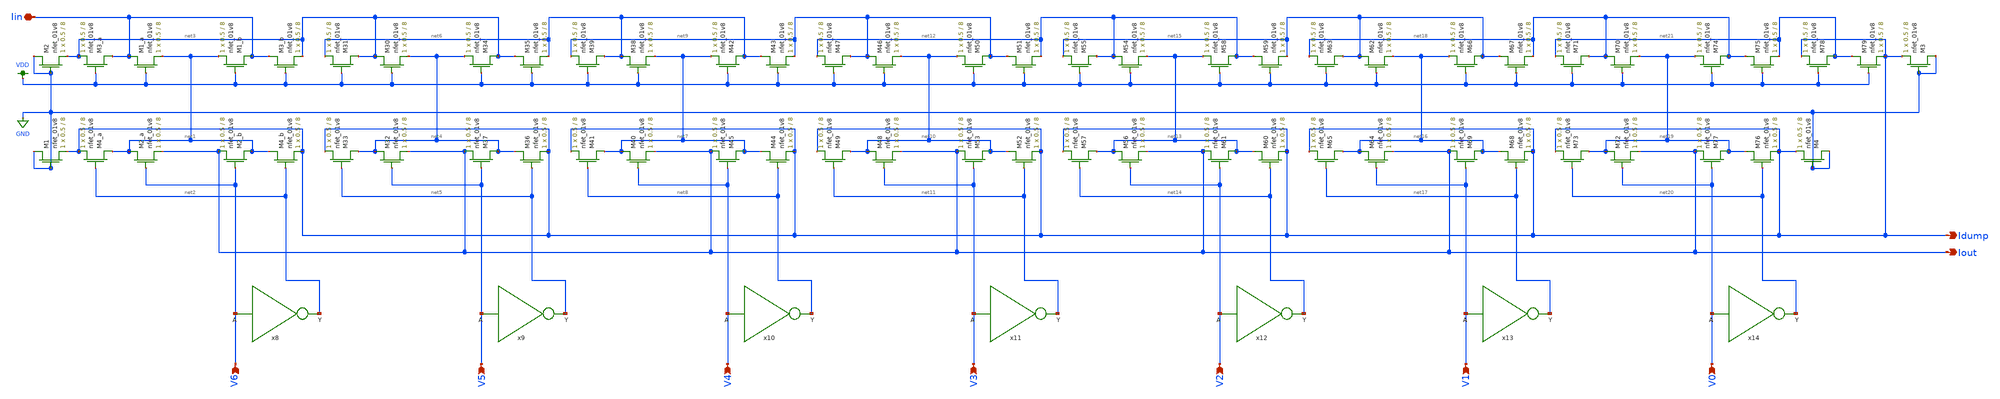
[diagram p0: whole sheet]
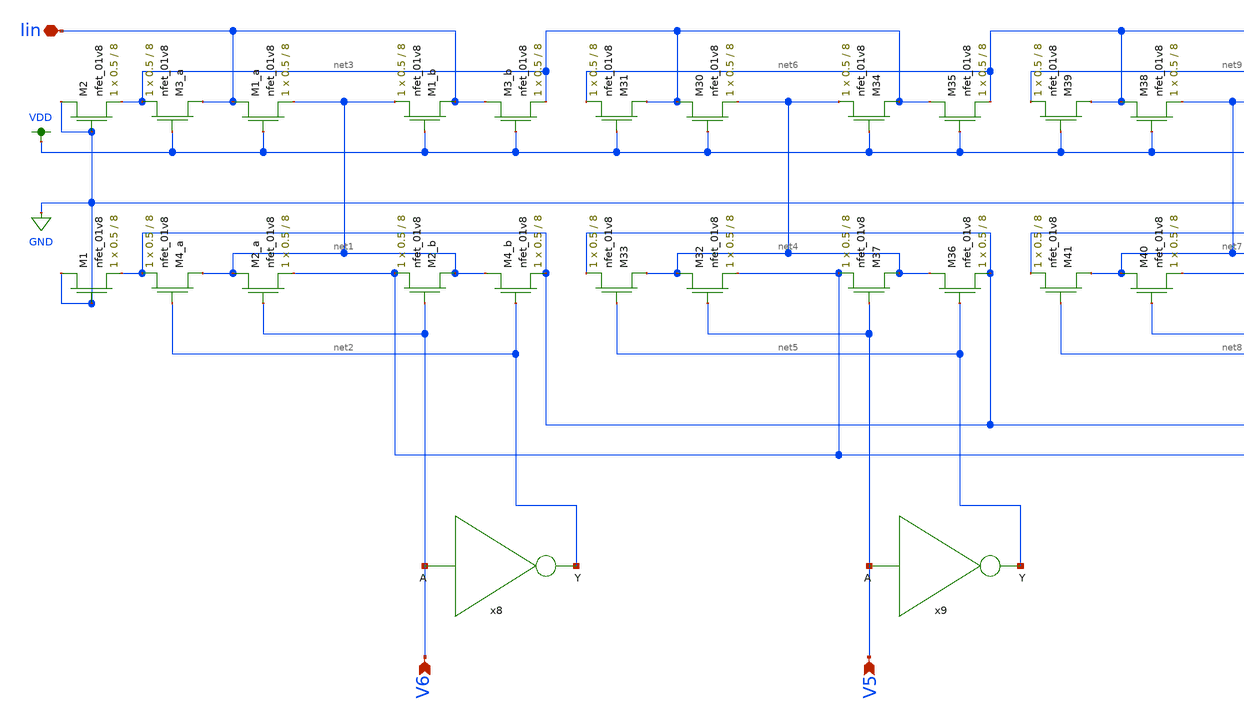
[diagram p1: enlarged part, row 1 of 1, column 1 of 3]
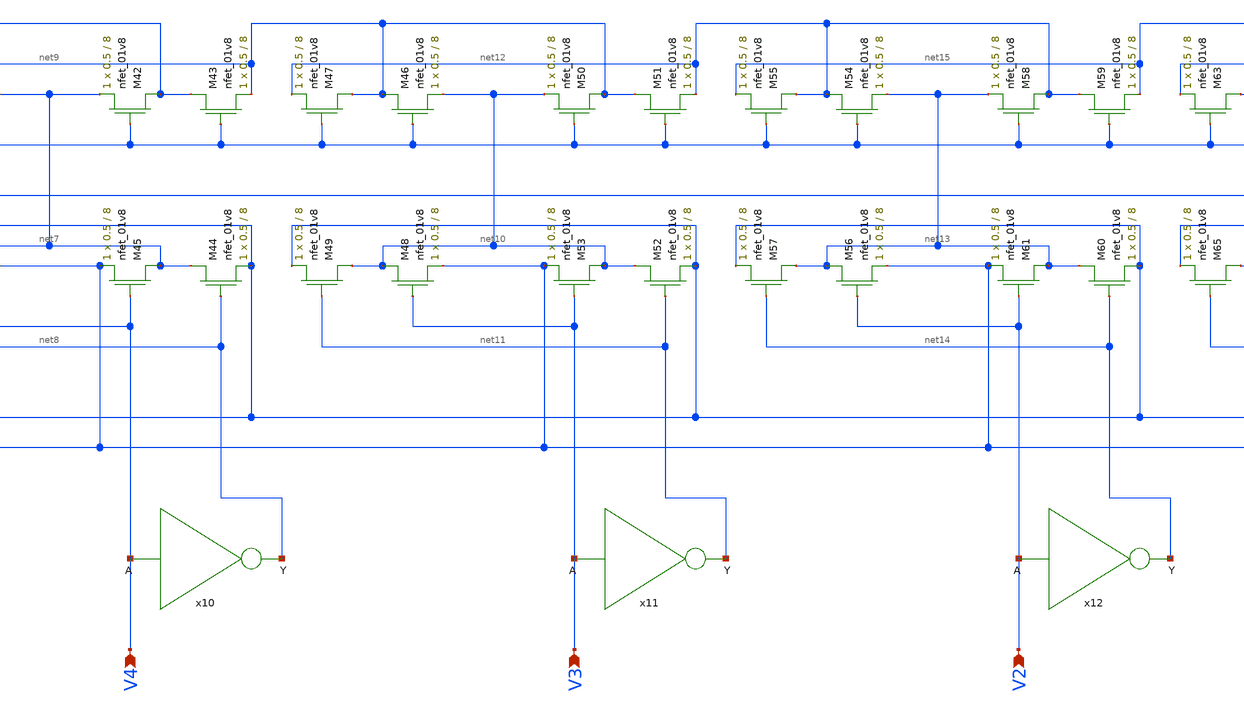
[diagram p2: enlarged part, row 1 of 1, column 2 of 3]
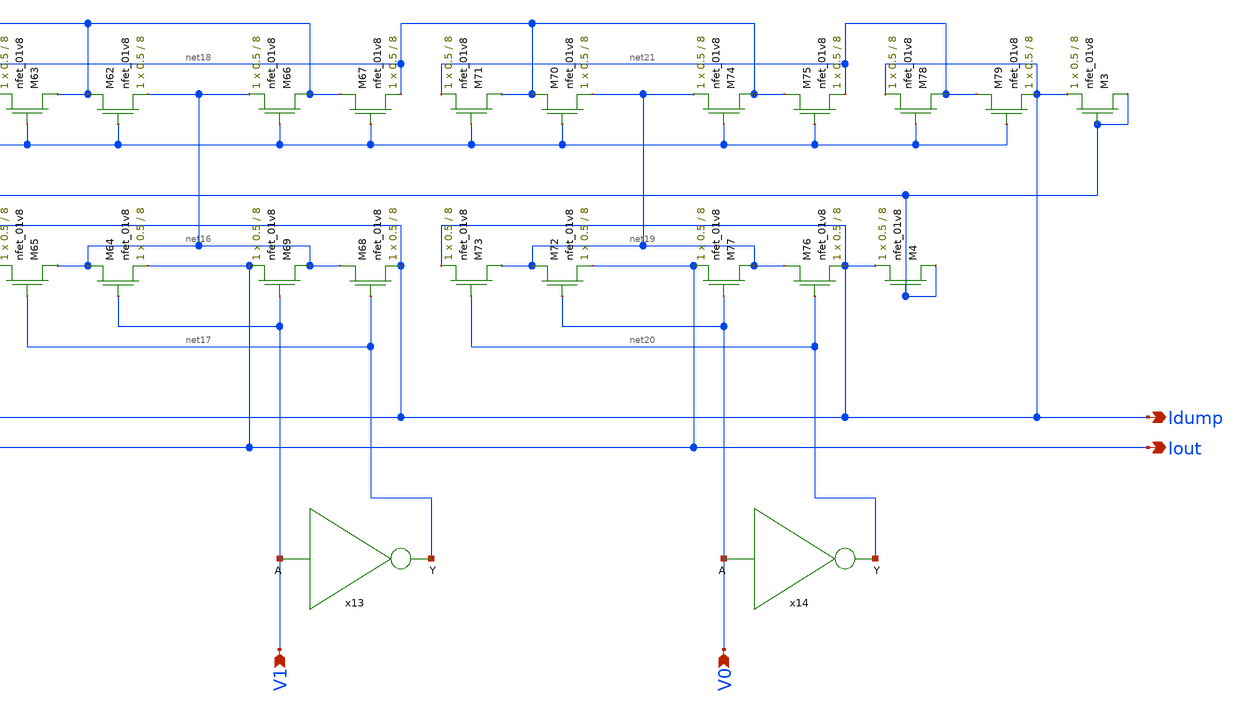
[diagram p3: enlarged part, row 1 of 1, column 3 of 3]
** sch_path: xschem/ladder_lds.sch
**.subckt ladder_lds Iin Idump Iout V6 V5 V4 V3 V2 V1 V0
*.iopin Iin
*.opin Idump
*.opin Iout
*.ipin V6
*.ipin V5
*.ipin V4
*.ipin V3
*.ipin V2
*.ipin V1
*.ipin V0
XM1_a Iin VDD net1 GND sky130_fd_pr__nfet_01v8 L=8 W=0.5 nf=1 ad='int((nf+1)/2) * W/nf * 0.29' as='int((nf+2)/2) * W/nf * 0.29'
+ pd='2*int((nf+1)/2) * (W/nf + 0.29)' ps='2*int((nf+2)/2) * (W/nf + 0.29)' nrd='0.29 / W' nrs='0.29 / W'
+ sa=0 sb=0 sd=0 mult=1 m=1
XM3_a Iin VDD net3 GND sky130_fd_pr__nfet_01v8 L=8 W=0.5 nf=1 ad='int((nf+1)/2) * W/nf * 0.29' as='int((nf+2)/2) * W/nf * 0.29'
+ pd='2*int((nf+1)/2) * (W/nf + 0.29)' ps='2*int((nf+2)/2) * (W/nf + 0.29)' nrd='0.29 / W' nrs='0.29 / W'
+ sa=0 sb=0 sd=0 mult=1 m=1
XM2_a net1 V6 Iout GND sky130_fd_pr__nfet_01v8 L=8 W=0.5 nf=1 ad='int((nf+1)/2) * W/nf * 0.29' as='int((nf+2)/2) * W/nf * 0.29'
+ pd='2*int((nf+1)/2) * (W/nf + 0.29)' ps='2*int((nf+2)/2) * (W/nf + 0.29)' nrd='0.29 / W' nrs='0.29 / W'
+ sa=0 sb=0 sd=0 mult=1 m=1
XM4_a net1 net2 Idump GND sky130_fd_pr__nfet_01v8 L=8 W=0.5 nf=1 ad='int((nf+1)/2) * W/nf * 0.29' as='int((nf+2)/2) * W/nf * 0.29'
+ pd='2*int((nf+1)/2) * (W/nf + 0.29)' ps='2*int((nf+2)/2) * (W/nf + 0.29)' nrd='0.29 / W' nrs='0.29 / W'
+ sa=0 sb=0 sd=0 mult=1 m=1
XM1_b Iin VDD net1 GND sky130_fd_pr__nfet_01v8 L=8 W=0.5 nf=1 ad='int((nf+1)/2) * W/nf * 0.29' as='int((nf+2)/2) * W/nf * 0.29'
+ pd='2*int((nf+1)/2) * (W/nf + 0.29)' ps='2*int((nf+2)/2) * (W/nf + 0.29)' nrd='0.29 / W' nrs='0.29 / W'
+ sa=0 sb=0 sd=0 mult=1 m=1
XM3_b Iin VDD net3 GND sky130_fd_pr__nfet_01v8 L=8 W=0.5 nf=1 ad='int((nf+1)/2) * W/nf * 0.29' as='int((nf+2)/2) * W/nf * 0.29'
+ pd='2*int((nf+1)/2) * (W/nf + 0.29)' ps='2*int((nf+2)/2) * (W/nf + 0.29)' nrd='0.29 / W' nrs='0.29 / W'
+ sa=0 sb=0 sd=0 mult=1 m=1
XM4_b net1 net2 Idump GND sky130_fd_pr__nfet_01v8 L=8 W=0.5 nf=1 ad='int((nf+1)/2) * W/nf * 0.29' as='int((nf+2)/2) * W/nf * 0.29'
+ pd='2*int((nf+1)/2) * (W/nf + 0.29)' ps='2*int((nf+2)/2) * (W/nf + 0.29)' nrd='0.29 / W' nrs='0.29 / W'
+ sa=0 sb=0 sd=0 mult=1 m=1
XM2_b net1 V6 Iout GND sky130_fd_pr__nfet_01v8 L=8 W=0.5 nf=1 ad='int((nf+1)/2) * W/nf * 0.29' as='int((nf+2)/2) * W/nf * 0.29'
+ pd='2*int((nf+1)/2) * (W/nf + 0.29)' ps='2*int((nf+2)/2) * (W/nf + 0.29)' nrd='0.29 / W' nrs='0.29 / W'
+ sa=0 sb=0 sd=0 mult=1 m=1
XM30 net3 VDD net4 GND sky130_fd_pr__nfet_01v8 L=8 W=0.5 nf=1 ad='int((nf+1)/2) * W/nf * 0.29' as='int((nf+2)/2) * W/nf * 0.29'
+ pd='2*int((nf+1)/2) * (W/nf + 0.29)' ps='2*int((nf+2)/2) * (W/nf + 0.29)' nrd='0.29 / W' nrs='0.29 / W'
+ sa=0 sb=0 sd=0 mult=1 m=1
XM31 net3 VDD net6 GND sky130_fd_pr__nfet_01v8 L=8 W=0.5 nf=1 ad='int((nf+1)/2) * W/nf * 0.29' as='int((nf+2)/2) * W/nf * 0.29'
+ pd='2*int((nf+1)/2) * (W/nf + 0.29)' ps='2*int((nf+2)/2) * (W/nf + 0.29)' nrd='0.29 / W' nrs='0.29 / W'
+ sa=0 sb=0 sd=0 mult=1 m=1
XM32 net4 V5 Iout GND sky130_fd_pr__nfet_01v8 L=8 W=0.5 nf=1 ad='int((nf+1)/2) * W/nf * 0.29' as='int((nf+2)/2) * W/nf * 0.29'
+ pd='2*int((nf+1)/2) * (W/nf + 0.29)' ps='2*int((nf+2)/2) * (W/nf + 0.29)' nrd='0.29 / W' nrs='0.29 / W'
+ sa=0 sb=0 sd=0 mult=1 m=1
XM33 net4 net5 Idump GND sky130_fd_pr__nfet_01v8 L=8 W=0.5 nf=1 ad='int((nf+1)/2) * W/nf * 0.29' as='int((nf+2)/2) * W/nf * 0.29'
+ pd='2*int((nf+1)/2) * (W/nf + 0.29)' ps='2*int((nf+2)/2) * (W/nf + 0.29)' nrd='0.29 / W' nrs='0.29 / W'
+ sa=0 sb=0 sd=0 mult=1 m=1
XM34 net3 VDD net4 GND sky130_fd_pr__nfet_01v8 L=8 W=0.5 nf=1 ad='int((nf+1)/2) * W/nf * 0.29' as='int((nf+2)/2) * W/nf * 0.29'
+ pd='2*int((nf+1)/2) * (W/nf + 0.29)' ps='2*int((nf+2)/2) * (W/nf + 0.29)' nrd='0.29 / W' nrs='0.29 / W'
+ sa=0 sb=0 sd=0 mult=1 m=1
XM35 net3 VDD net6 GND sky130_fd_pr__nfet_01v8 L=8 W=0.5 nf=1 ad='int((nf+1)/2) * W/nf * 0.29' as='int((nf+2)/2) * W/nf * 0.29'
+ pd='2*int((nf+1)/2) * (W/nf + 0.29)' ps='2*int((nf+2)/2) * (W/nf + 0.29)' nrd='0.29 / W' nrs='0.29 / W'
+ sa=0 sb=0 sd=0 mult=1 m=1
XM36 net4 net5 Idump GND sky130_fd_pr__nfet_01v8 L=8 W=0.5 nf=1 ad='int((nf+1)/2) * W/nf * 0.29' as='int((nf+2)/2) * W/nf * 0.29'
+ pd='2*int((nf+1)/2) * (W/nf + 0.29)' ps='2*int((nf+2)/2) * (W/nf + 0.29)' nrd='0.29 / W' nrs='0.29 / W'
+ sa=0 sb=0 sd=0 mult=1 m=1
XM37 net4 V5 Iout GND sky130_fd_pr__nfet_01v8 L=8 W=0.5 nf=1 ad='int((nf+1)/2) * W/nf * 0.29' as='int((nf+2)/2) * W/nf * 0.29'
+ pd='2*int((nf+1)/2) * (W/nf + 0.29)' ps='2*int((nf+2)/2) * (W/nf + 0.29)' nrd='0.29 / W' nrs='0.29 / W'
+ sa=0 sb=0 sd=0 mult=1 m=1
XM38 net6 VDD net7 GND sky130_fd_pr__nfet_01v8 L=8 W=0.5 nf=1 ad='int((nf+1)/2) * W/nf * 0.29' as='int((nf+2)/2) * W/nf * 0.29'
+ pd='2*int((nf+1)/2) * (W/nf + 0.29)' ps='2*int((nf+2)/2) * (W/nf + 0.29)' nrd='0.29 / W' nrs='0.29 / W'
+ sa=0 sb=0 sd=0 mult=1 m=1
XM39 net6 VDD net9 GND sky130_fd_pr__nfet_01v8 L=8 W=0.5 nf=1 ad='int((nf+1)/2) * W/nf * 0.29' as='int((nf+2)/2) * W/nf * 0.29'
+ pd='2*int((nf+1)/2) * (W/nf + 0.29)' ps='2*int((nf+2)/2) * (W/nf + 0.29)' nrd='0.29 / W' nrs='0.29 / W'
+ sa=0 sb=0 sd=0 mult=1 m=1
XM40 net7 V4 Iout GND sky130_fd_pr__nfet_01v8 L=8 W=0.5 nf=1 ad='int((nf+1)/2) * W/nf * 0.29' as='int((nf+2)/2) * W/nf * 0.29'
+ pd='2*int((nf+1)/2) * (W/nf + 0.29)' ps='2*int((nf+2)/2) * (W/nf + 0.29)' nrd='0.29 / W' nrs='0.29 / W'
+ sa=0 sb=0 sd=0 mult=1 m=1
XM41 net7 net8 Idump GND sky130_fd_pr__nfet_01v8 L=8 W=0.5 nf=1 ad='int((nf+1)/2) * W/nf * 0.29' as='int((nf+2)/2) * W/nf * 0.29'
+ pd='2*int((nf+1)/2) * (W/nf + 0.29)' ps='2*int((nf+2)/2) * (W/nf + 0.29)' nrd='0.29 / W' nrs='0.29 / W'
+ sa=0 sb=0 sd=0 mult=1 m=1
XM42 net6 VDD net7 GND sky130_fd_pr__nfet_01v8 L=8 W=0.5 nf=1 ad='int((nf+1)/2) * W/nf * 0.29' as='int((nf+2)/2) * W/nf * 0.29'
+ pd='2*int((nf+1)/2) * (W/nf + 0.29)' ps='2*int((nf+2)/2) * (W/nf + 0.29)' nrd='0.29 / W' nrs='0.29 / W'
+ sa=0 sb=0 sd=0 mult=1 m=1
XM43 net6 VDD net9 GND sky130_fd_pr__nfet_01v8 L=8 W=0.5 nf=1 ad='int((nf+1)/2) * W/nf * 0.29' as='int((nf+2)/2) * W/nf * 0.29'
+ pd='2*int((nf+1)/2) * (W/nf + 0.29)' ps='2*int((nf+2)/2) * (W/nf + 0.29)' nrd='0.29 / W' nrs='0.29 / W'
+ sa=0 sb=0 sd=0 mult=1 m=1
XM44 net7 net8 Idump GND sky130_fd_pr__nfet_01v8 L=8 W=0.5 nf=1 ad='int((nf+1)/2) * W/nf * 0.29' as='int((nf+2)/2) * W/nf * 0.29'
+ pd='2*int((nf+1)/2) * (W/nf + 0.29)' ps='2*int((nf+2)/2) * (W/nf + 0.29)' nrd='0.29 / W' nrs='0.29 / W'
+ sa=0 sb=0 sd=0 mult=1 m=1
XM45 net7 V4 Iout GND sky130_fd_pr__nfet_01v8 L=8 W=0.5 nf=1 ad='int((nf+1)/2) * W/nf * 0.29' as='int((nf+2)/2) * W/nf * 0.29'
+ pd='2*int((nf+1)/2) * (W/nf + 0.29)' ps='2*int((nf+2)/2) * (W/nf + 0.29)' nrd='0.29 / W' nrs='0.29 / W'
+ sa=0 sb=0 sd=0 mult=1 m=1
XM46 net9 VDD net10 GND sky130_fd_pr__nfet_01v8 L=8 W=0.5 nf=1 ad='int((nf+1)/2) * W/nf * 0.29' as='int((nf+2)/2) * W/nf * 0.29'
+ pd='2*int((nf+1)/2) * (W/nf + 0.29)' ps='2*int((nf+2)/2) * (W/nf + 0.29)' nrd='0.29 / W' nrs='0.29 / W'
+ sa=0 sb=0 sd=0 mult=1 m=1
XM47 net9 VDD net12 GND sky130_fd_pr__nfet_01v8 L=8 W=0.5 nf=1 ad='int((nf+1)/2) * W/nf * 0.29' as='int((nf+2)/2) * W/nf * 0.29'
+ pd='2*int((nf+1)/2) * (W/nf + 0.29)' ps='2*int((nf+2)/2) * (W/nf + 0.29)' nrd='0.29 / W' nrs='0.29 / W'
+ sa=0 sb=0 sd=0 mult=1 m=1
XM48 net10 V3 Iout GND sky130_fd_pr__nfet_01v8 L=8 W=0.5 nf=1 ad='int((nf+1)/2) * W/nf * 0.29' as='int((nf+2)/2) * W/nf * 0.29'
+ pd='2*int((nf+1)/2) * (W/nf + 0.29)' ps='2*int((nf+2)/2) * (W/nf + 0.29)' nrd='0.29 / W' nrs='0.29 / W'
+ sa=0 sb=0 sd=0 mult=1 m=1
XM49 net10 net11 Idump GND sky130_fd_pr__nfet_01v8 L=8 W=0.5 nf=1 ad='int((nf+1)/2) * W/nf * 0.29' as='int((nf+2)/2) * W/nf * 0.29'
+ pd='2*int((nf+1)/2) * (W/nf + 0.29)' ps='2*int((nf+2)/2) * (W/nf + 0.29)' nrd='0.29 / W' nrs='0.29 / W'
+ sa=0 sb=0 sd=0 mult=1 m=1
XM50 net9 VDD net10 GND sky130_fd_pr__nfet_01v8 L=8 W=0.5 nf=1 ad='int((nf+1)/2) * W/nf * 0.29' as='int((nf+2)/2) * W/nf * 0.29'
+ pd='2*int((nf+1)/2) * (W/nf + 0.29)' ps='2*int((nf+2)/2) * (W/nf + 0.29)' nrd='0.29 / W' nrs='0.29 / W'
+ sa=0 sb=0 sd=0 mult=1 m=1
XM51 net9 VDD net12 GND sky130_fd_pr__nfet_01v8 L=8 W=0.5 nf=1 ad='int((nf+1)/2) * W/nf * 0.29' as='int((nf+2)/2) * W/nf * 0.29'
+ pd='2*int((nf+1)/2) * (W/nf + 0.29)' ps='2*int((nf+2)/2) * (W/nf + 0.29)' nrd='0.29 / W' nrs='0.29 / W'
+ sa=0 sb=0 sd=0 mult=1 m=1
XM52 net10 net11 Idump GND sky130_fd_pr__nfet_01v8 L=8 W=0.5 nf=1 ad='int((nf+1)/2) * W/nf * 0.29' as='int((nf+2)/2) * W/nf * 0.29'
+ pd='2*int((nf+1)/2) * (W/nf + 0.29)' ps='2*int((nf+2)/2) * (W/nf + 0.29)' nrd='0.29 / W' nrs='0.29 / W'
+ sa=0 sb=0 sd=0 mult=1 m=1
XM53 net10 V3 Iout GND sky130_fd_pr__nfet_01v8 L=8 W=0.5 nf=1 ad='int((nf+1)/2) * W/nf * 0.29' as='int((nf+2)/2) * W/nf * 0.29'
+ pd='2*int((nf+1)/2) * (W/nf + 0.29)' ps='2*int((nf+2)/2) * (W/nf + 0.29)' nrd='0.29 / W' nrs='0.29 / W'
+ sa=0 sb=0 sd=0 mult=1 m=1
XM54 net12 VDD net13 GND sky130_fd_pr__nfet_01v8 L=8 W=0.5 nf=1 ad='int((nf+1)/2) * W/nf * 0.29' as='int((nf+2)/2) * W/nf * 0.29'
+ pd='2*int((nf+1)/2) * (W/nf + 0.29)' ps='2*int((nf+2)/2) * (W/nf + 0.29)' nrd='0.29 / W' nrs='0.29 / W'
+ sa=0 sb=0 sd=0 mult=1 m=1
XM55 net12 VDD net15 GND sky130_fd_pr__nfet_01v8 L=8 W=0.5 nf=1 ad='int((nf+1)/2) * W/nf * 0.29' as='int((nf+2)/2) * W/nf * 0.29'
+ pd='2*int((nf+1)/2) * (W/nf + 0.29)' ps='2*int((nf+2)/2) * (W/nf + 0.29)' nrd='0.29 / W' nrs='0.29 / W'
+ sa=0 sb=0 sd=0 mult=1 m=1
XM56 net13 V2 Iout GND sky130_fd_pr__nfet_01v8 L=8 W=0.5 nf=1 ad='int((nf+1)/2) * W/nf * 0.29' as='int((nf+2)/2) * W/nf * 0.29'
+ pd='2*int((nf+1)/2) * (W/nf + 0.29)' ps='2*int((nf+2)/2) * (W/nf + 0.29)' nrd='0.29 / W' nrs='0.29 / W'
+ sa=0 sb=0 sd=0 mult=1 m=1
XM57 net13 net14 Idump GND sky130_fd_pr__nfet_01v8 L=8 W=0.5 nf=1 ad='int((nf+1)/2) * W/nf * 0.29' as='int((nf+2)/2) * W/nf * 0.29'
+ pd='2*int((nf+1)/2) * (W/nf + 0.29)' ps='2*int((nf+2)/2) * (W/nf + 0.29)' nrd='0.29 / W' nrs='0.29 / W'
+ sa=0 sb=0 sd=0 mult=1 m=1
XM58 net12 VDD net13 GND sky130_fd_pr__nfet_01v8 L=8 W=0.5 nf=1 ad='int((nf+1)/2) * W/nf * 0.29' as='int((nf+2)/2) * W/nf * 0.29'
+ pd='2*int((nf+1)/2) * (W/nf + 0.29)' ps='2*int((nf+2)/2) * (W/nf + 0.29)' nrd='0.29 / W' nrs='0.29 / W'
+ sa=0 sb=0 sd=0 mult=1 m=1
XM59 net12 VDD net15 GND sky130_fd_pr__nfet_01v8 L=8 W=0.5 nf=1 ad='int((nf+1)/2) * W/nf * 0.29' as='int((nf+2)/2) * W/nf * 0.29'
+ pd='2*int((nf+1)/2) * (W/nf + 0.29)' ps='2*int((nf+2)/2) * (W/nf + 0.29)' nrd='0.29 / W' nrs='0.29 / W'
+ sa=0 sb=0 sd=0 mult=1 m=1
XM60 net13 net14 Idump GND sky130_fd_pr__nfet_01v8 L=8 W=0.5 nf=1 ad='int((nf+1)/2) * W/nf * 0.29' as='int((nf+2)/2) * W/nf * 0.29'
+ pd='2*int((nf+1)/2) * (W/nf + 0.29)' ps='2*int((nf+2)/2) * (W/nf + 0.29)' nrd='0.29 / W' nrs='0.29 / W'
+ sa=0 sb=0 sd=0 mult=1 m=1
XM61 net13 V2 Iout GND sky130_fd_pr__nfet_01v8 L=8 W=0.5 nf=1 ad='int((nf+1)/2) * W/nf * 0.29' as='int((nf+2)/2) * W/nf * 0.29'
+ pd='2*int((nf+1)/2) * (W/nf + 0.29)' ps='2*int((nf+2)/2) * (W/nf + 0.29)' nrd='0.29 / W' nrs='0.29 / W'
+ sa=0 sb=0 sd=0 mult=1 m=1
XM62 net15 VDD net16 GND sky130_fd_pr__nfet_01v8 L=8 W=0.5 nf=1 ad='int((nf+1)/2) * W/nf * 0.29' as='int((nf+2)/2) * W/nf * 0.29'
+ pd='2*int((nf+1)/2) * (W/nf + 0.29)' ps='2*int((nf+2)/2) * (W/nf + 0.29)' nrd='0.29 / W' nrs='0.29 / W'
+ sa=0 sb=0 sd=0 mult=1 m=1
XM63 net15 VDD net18 GND sky130_fd_pr__nfet_01v8 L=8 W=0.5 nf=1 ad='int((nf+1)/2) * W/nf * 0.29' as='int((nf+2)/2) * W/nf * 0.29'
+ pd='2*int((nf+1)/2) * (W/nf + 0.29)' ps='2*int((nf+2)/2) * (W/nf + 0.29)' nrd='0.29 / W' nrs='0.29 / W'
+ sa=0 sb=0 sd=0 mult=1 m=1
XM64 net16 V1 Iout GND sky130_fd_pr__nfet_01v8 L=8 W=0.5 nf=1 ad='int((nf+1)/2) * W/nf * 0.29' as='int((nf+2)/2) * W/nf * 0.29'
+ pd='2*int((nf+1)/2) * (W/nf + 0.29)' ps='2*int((nf+2)/2) * (W/nf + 0.29)' nrd='0.29 / W' nrs='0.29 / W'
+ sa=0 sb=0 sd=0 mult=1 m=1
XM65 net16 net17 Idump GND sky130_fd_pr__nfet_01v8 L=8 W=0.5 nf=1 ad='int((nf+1)/2) * W/nf * 0.29' as='int((nf+2)/2) * W/nf * 0.29'
+ pd='2*int((nf+1)/2) * (W/nf + 0.29)' ps='2*int((nf+2)/2) * (W/nf + 0.29)' nrd='0.29 / W' nrs='0.29 / W'
+ sa=0 sb=0 sd=0 mult=1 m=1
XM66 net15 VDD net16 GND sky130_fd_pr__nfet_01v8 L=8 W=0.5 nf=1 ad='int((nf+1)/2) * W/nf * 0.29' as='int((nf+2)/2) * W/nf * 0.29'
+ pd='2*int((nf+1)/2) * (W/nf + 0.29)' ps='2*int((nf+2)/2) * (W/nf + 0.29)' nrd='0.29 / W' nrs='0.29 / W'
+ sa=0 sb=0 sd=0 mult=1 m=1
XM67 net15 VDD net18 GND sky130_fd_pr__nfet_01v8 L=8 W=0.5 nf=1 ad='int((nf+1)/2) * W/nf * 0.29' as='int((nf+2)/2) * W/nf * 0.29'
+ pd='2*int((nf+1)/2) * (W/nf + 0.29)' ps='2*int((nf+2)/2) * (W/nf + 0.29)' nrd='0.29 / W' nrs='0.29 / W'
+ sa=0 sb=0 sd=0 mult=1 m=1
XM68 net16 net17 Idump GND sky130_fd_pr__nfet_01v8 L=8 W=0.5 nf=1 ad='int((nf+1)/2) * W/nf * 0.29' as='int((nf+2)/2) * W/nf * 0.29'
+ pd='2*int((nf+1)/2) * (W/nf + 0.29)' ps='2*int((nf+2)/2) * (W/nf + 0.29)' nrd='0.29 / W' nrs='0.29 / W'
+ sa=0 sb=0 sd=0 mult=1 m=1
XM69 net16 V1 Iout GND sky130_fd_pr__nfet_01v8 L=8 W=0.5 nf=1 ad='int((nf+1)/2) * W/nf * 0.29' as='int((nf+2)/2) * W/nf * 0.29'
+ pd='2*int((nf+1)/2) * (W/nf + 0.29)' ps='2*int((nf+2)/2) * (W/nf + 0.29)' nrd='0.29 / W' nrs='0.29 / W'
+ sa=0 sb=0 sd=0 mult=1 m=1
XM70 net18 VDD net19 GND sky130_fd_pr__nfet_01v8 L=8 W=0.5 nf=1 ad='int((nf+1)/2) * W/nf * 0.29' as='int((nf+2)/2) * W/nf * 0.29'
+ pd='2*int((nf+1)/2) * (W/nf + 0.29)' ps='2*int((nf+2)/2) * (W/nf + 0.29)' nrd='0.29 / W' nrs='0.29 / W'
+ sa=0 sb=0 sd=0 mult=1 m=1
XM71 net18 VDD net21 GND sky130_fd_pr__nfet_01v8 L=8 W=0.5 nf=1 ad='int((nf+1)/2) * W/nf * 0.29' as='int((nf+2)/2) * W/nf * 0.29'
+ pd='2*int((nf+1)/2) * (W/nf + 0.29)' ps='2*int((nf+2)/2) * (W/nf + 0.29)' nrd='0.29 / W' nrs='0.29 / W'
+ sa=0 sb=0 sd=0 mult=1 m=1
XM72 net19 V0 Iout GND sky130_fd_pr__nfet_01v8 L=8 W=0.5 nf=1 ad='int((nf+1)/2) * W/nf * 0.29' as='int((nf+2)/2) * W/nf * 0.29'
+ pd='2*int((nf+1)/2) * (W/nf + 0.29)' ps='2*int((nf+2)/2) * (W/nf + 0.29)' nrd='0.29 / W' nrs='0.29 / W'
+ sa=0 sb=0 sd=0 mult=1 m=1
XM73 net19 net20 Idump GND sky130_fd_pr__nfet_01v8 L=8 W=0.5 nf=1 ad='int((nf+1)/2) * W/nf * 0.29' as='int((nf+2)/2) * W/nf * 0.29'
+ pd='2*int((nf+1)/2) * (W/nf + 0.29)' ps='2*int((nf+2)/2) * (W/nf + 0.29)' nrd='0.29 / W' nrs='0.29 / W'
+ sa=0 sb=0 sd=0 mult=1 m=1
XM74 net18 VDD net19 GND sky130_fd_pr__nfet_01v8 L=8 W=0.5 nf=1 ad='int((nf+1)/2) * W/nf * 0.29' as='int((nf+2)/2) * W/nf * 0.29'
+ pd='2*int((nf+1)/2) * (W/nf + 0.29)' ps='2*int((nf+2)/2) * (W/nf + 0.29)' nrd='0.29 / W' nrs='0.29 / W'
+ sa=0 sb=0 sd=0 mult=1 m=1
XM75 net18 VDD net21 GND sky130_fd_pr__nfet_01v8 L=8 W=0.5 nf=1 ad='int((nf+1)/2) * W/nf * 0.29' as='int((nf+2)/2) * W/nf * 0.29'
+ pd='2*int((nf+1)/2) * (W/nf + 0.29)' ps='2*int((nf+2)/2) * (W/nf + 0.29)' nrd='0.29 / W' nrs='0.29 / W'
+ sa=0 sb=0 sd=0 mult=1 m=1
XM76 net19 net20 Idump GND sky130_fd_pr__nfet_01v8 L=8 W=0.5 nf=1 ad='int((nf+1)/2) * W/nf * 0.29' as='int((nf+2)/2) * W/nf * 0.29'
+ pd='2*int((nf+1)/2) * (W/nf + 0.29)' ps='2*int((nf+2)/2) * (W/nf + 0.29)' nrd='0.29 / W' nrs='0.29 / W'
+ sa=0 sb=0 sd=0 mult=1 m=1
XM77 net19 V0 Iout GND sky130_fd_pr__nfet_01v8 L=8 W=0.5 nf=1 ad='int((nf+1)/2) * W/nf * 0.29' as='int((nf+2)/2) * W/nf * 0.29'
+ pd='2*int((nf+1)/2) * (W/nf + 0.29)' ps='2*int((nf+2)/2) * (W/nf + 0.29)' nrd='0.29 / W' nrs='0.29 / W'
+ sa=0 sb=0 sd=0 mult=1 m=1
XM78 net21 VDD Idump GND sky130_fd_pr__nfet_01v8 L=8 W=0.5 nf=1 ad='int((nf+1)/2) * W/nf * 0.29' as='int((nf+2)/2) * W/nf * 0.29'
+ pd='2*int((nf+1)/2) * (W/nf + 0.29)' ps='2*int((nf+2)/2) * (W/nf + 0.29)' nrd='0.29 / W' nrs='0.29 / W'
+ sa=0 sb=0 sd=0 mult=1 m=1
XM79 net21 VDD Idump GND sky130_fd_pr__nfet_01v8 L=8 W=0.5 nf=1 ad='int((nf+1)/2) * W/nf * 0.29' as='int((nf+2)/2) * W/nf * 0.29'
+ pd='2*int((nf+1)/2) * (W/nf + 0.29)' ps='2*int((nf+2)/2) * (W/nf + 0.29)' nrd='0.29 / W' nrs='0.29 / W'
+ sa=0 sb=0 sd=0 mult=1 m=1
x8 net2 V6 inverter
x9 net5 V5 inverter
x10 net8 V4 inverter
x11 net11 V3 inverter
x12 net14 V2 inverter
x13 net17 V1 inverter
x14 net20 V0 inverter
XM1 GND GND Idump GND sky130_fd_pr__nfet_01v8 L=8 W=0.5 nf=1 ad='int((nf+1)/2) * W/nf * 0.29' as='int((nf+2)/2) * W/nf * 0.29'
+ pd='2*int((nf+1)/2) * (W/nf + 0.29)' ps='2*int((nf+2)/2) * (W/nf + 0.29)' nrd='0.29 / W' nrs='0.29 / W'
+ sa=0 sb=0 sd=0 mult=1 m=1
XM2 GND GND net3 GND sky130_fd_pr__nfet_01v8 L=8 W=0.5 nf=1 ad='int((nf+1)/2) * W/nf * 0.29' as='int((nf+2)/2) * W/nf * 0.29'
+ pd='2*int((nf+1)/2) * (W/nf + 0.29)' ps='2*int((nf+2)/2) * (W/nf + 0.29)' nrd='0.29 / W' nrs='0.29 / W'
+ sa=0 sb=0 sd=0 mult=1 m=1
XM3 GND GND Idump GND sky130_fd_pr__nfet_01v8 L=8 W=0.5 nf=1 ad='int((nf+1)/2) * W/nf * 0.29' as='int((nf+2)/2) * W/nf * 0.29'
+ pd='2*int((nf+1)/2) * (W/nf + 0.29)' ps='2*int((nf+2)/2) * (W/nf + 0.29)' nrd='0.29 / W' nrs='0.29 / W'
+ sa=0 sb=0 sd=0 mult=1 m=1
XM4 GND GND Idump GND sky130_fd_pr__nfet_01v8 L=8 W=0.5 nf=1 ad='int((nf+1)/2) * W/nf * 0.29' as='int((nf+2)/2) * W/nf * 0.29'
+ pd='2*int((nf+1)/2) * (W/nf + 0.29)' ps='2*int((nf+2)/2) * (W/nf + 0.29)' nrd='0.29 / W' nrs='0.29 / W'
+ sa=0 sb=0 sd=0 mult=1 m=1
**.ends

* expanding   symbol:  ./inverter.sym # of pins=2
** sym_path: xschem/inverter.sym
** sch_path: xschem/inverter.sch
.subckt inverter Y A
*.ipin A
*.opin Y
XM1 Y A VDD VDD sky130_fd_pr__pfet_01v8 L=0.15 W=1 nf=1 ad='int((nf+1)/2) * W/nf * 0.29' as='int((nf+2)/2) * W/nf * 0.29'
+ pd='2*int((nf+1)/2) * (W/nf + 0.29)' ps='2*int((nf+2)/2) * (W/nf + 0.29)' nrd='0.29 / W' nrs='0.29 / W'
+ sa=0 sb=0 sd=0 mult=1 m=1
XM2 Y A GND GND sky130_fd_pr__nfet_01v8 L=0.15 W=1 nf=1 ad='int((nf+1)/2) * W/nf * 0.29' as='int((nf+2)/2) * W/nf * 0.29'
+ pd='2*int((nf+1)/2) * (W/nf + 0.29)' ps='2*int((nf+2)/2) * (W/nf + 0.29)' nrd='0.29 / W' nrs='0.29 / W'
+ sa=0 sb=0 sd=0 mult=1 m=1
.ends

.GLOBAL VDD
.GLOBAL GND
.end
